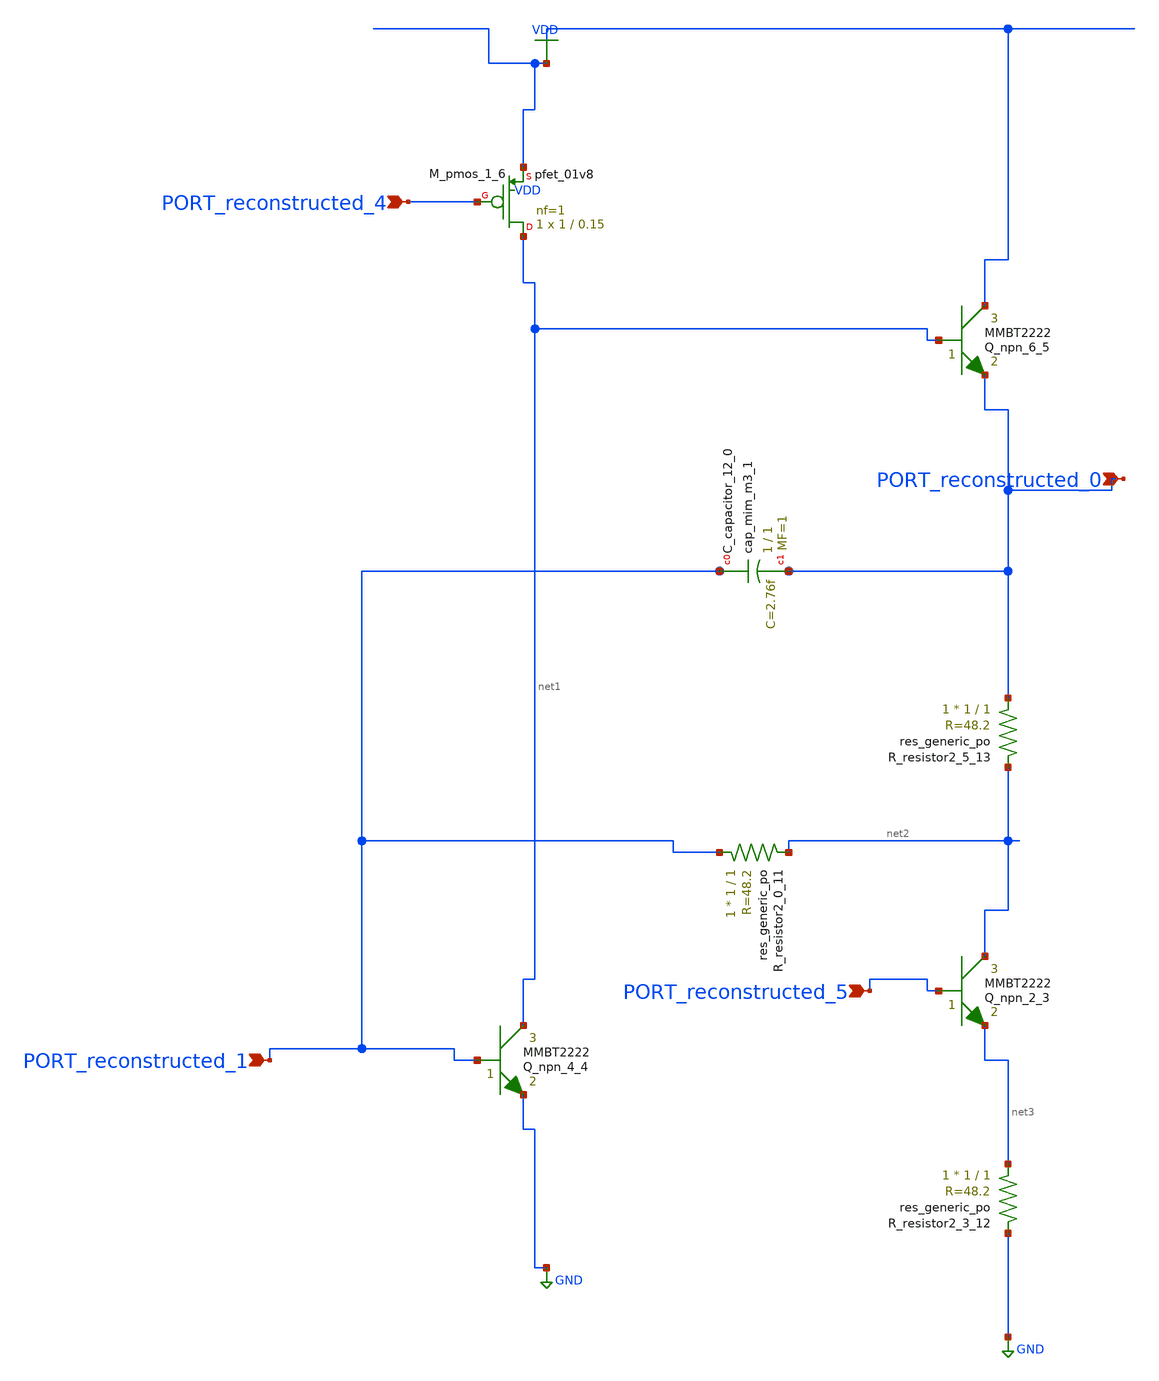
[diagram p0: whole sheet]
** sch_path: schematics/SchemGen/10_1016_j_nima_2022_167570_07_002.sch
**.subckt 10_1016_j_nima_2022_167570_07_002 PORT_reconstructed_1 PORT_reconstructed_5
*+ PORT_reconstructed_0 PORT_reconstructed_4
*.ipin PORT_reconstructed_1
*.ipin PORT_reconstructed_5
*.ipin PORT_reconstructed_0
*.ipin PORT_reconstructed_4
XC_capacitor_12_0 PORT_reconstructed_1 PORT_reconstructed_0 sky130_fd_pr__cap_mim_m3_1 W=1 L=1 MF=1
+ m=1
Q_npn_2_3 net2 PORT_reconstructed_5 net3 MMBT2222 area=1 m=1
Q_npn_4_4 net1 PORT_reconstructed_1 GND MMBT2222 area=1 m=1
Q_npn_6_5 VDD net1 PORT_reconstructed_0 MMBT2222 area=1 m=1
XM_pmos_1_6 net1 PORT_reconstructed_4 VDD VDD sky130_fd_pr__pfet_01v8 L=0.15 W=1 nf=1 ad='int((1 + 1)/2) * 1 / 1 * 0.29'
+ as='int((1 + 2)/2) * 1 / 1 * 0.29' pd='2*int((1 + 1)/2) * (1 / 1 + 0.29)' ps='2*int((1 + 2)/2) * (1 / 1 + 0.29)'
+ nrd='0.29 / 1 ' nrs='0.29 / 1 ' sa=0 sb=0 sd=0 mult=1 m=1
XR_resistor2_0_11 PORT_reconstructed_1 net2 sky130_fd_pr__res_generic_po W=1 L=1 m=1
XR_resistor2_3_12 net3 GND sky130_fd_pr__res_generic_po W=1 L=1 m=1
XR_resistor2_5_13 PORT_reconstructed_0 net2 sky130_fd_pr__res_generic_po W=1 L=1 m=1
**.ends
.GLOBAL GND
.GLOBAL VDD
.end
